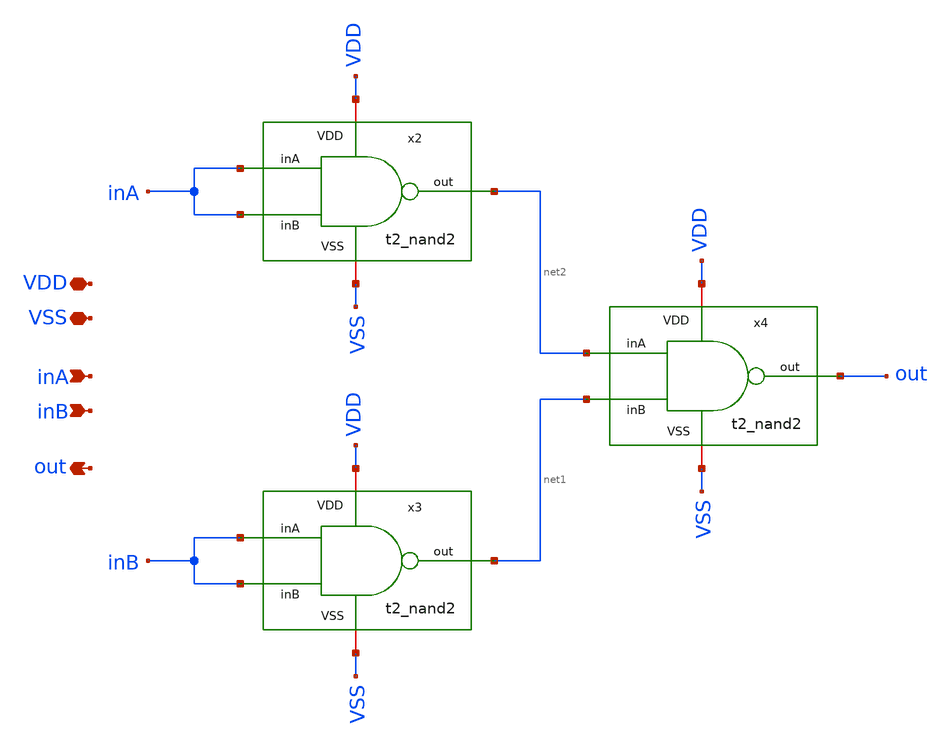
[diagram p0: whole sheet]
** sch_path: Team Designs/Team 2 Design/design_data/xschem/t2_or2.sch
**.subckt t2_or2 VSS inA inB out VDD
*.iopin VSS
*.ipin inA
*.ipin inB
*.opin out
*.iopin VDD
x2 VDD inA inA net2 VSS t2_nand2
x3 VDD inB inB net1 VSS t2_nand2
x4 VDD net2 net1 out VSS t2_nand2
**.ends

* expanding   symbol:  t2_nand2.sym # of pins=5
** sym_path: Team 2 Design/design_data/xschem/t2_nand2.sym
** sch_path: Team 2 Design/design_data/xschem/t2_nand2.sch
.subckt t2_nand2 VDD inA inB out VSS
*.iopin VSS
*.ipin inA
*.ipin inB
*.opin out
*.iopin VDD
XM1 out inA VDD VDD sg13_lv_pmos w=1u l=0.45u ng=1 m=1 mm_ok=1
XM2 out inB VDD VDD sg13_lv_pmos w=1u l=0.45u ng=1 m=1 mm_ok=1
XM3 out inB net1 VSS sg13_lv_nmos w=0.5u l=0.45u ng=1 m=1 mm_ok=1
XM4 net1 inA VSS VSS sg13_lv_nmos w=0.5u l=0.45u ng=1 m=1 mm_ok=1
.ends

.end
